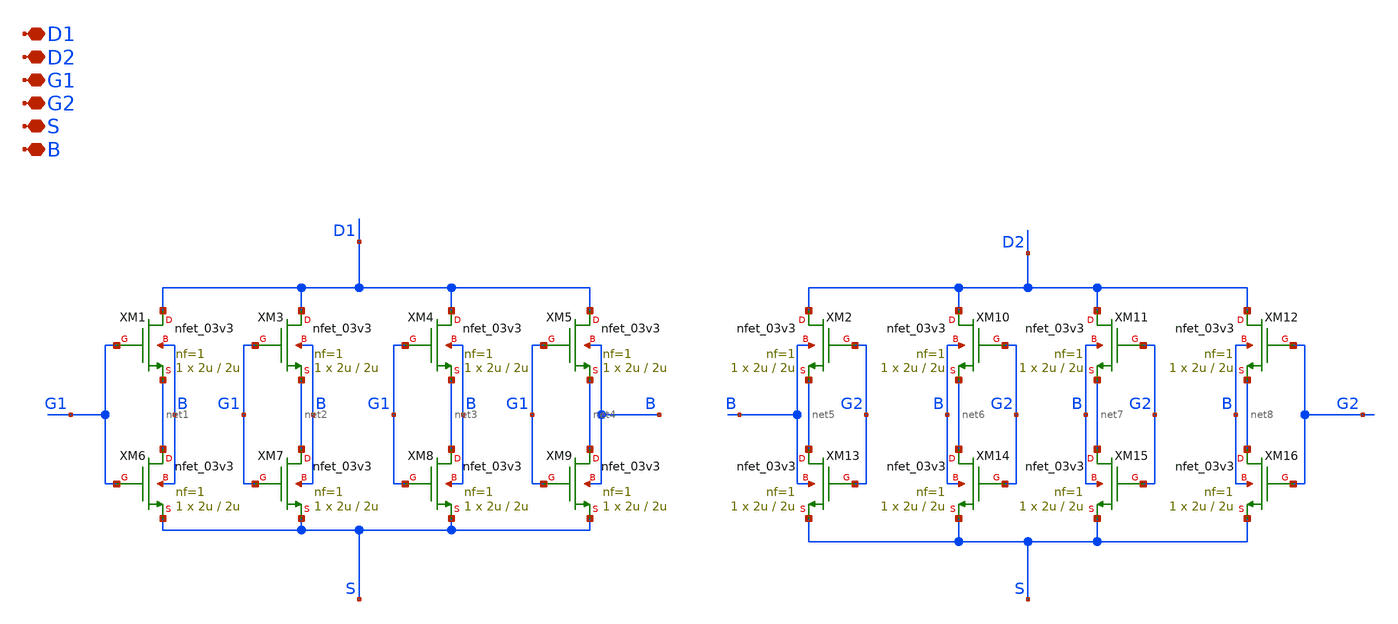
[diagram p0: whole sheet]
** sch_path: TIA/PseudoResistor/DiffN_nfets.sch
**.subckt DiffN_nfets D1 D2 G1 G2 S B
*.iopin D1
*.iopin D2
*.iopin G1
*.iopin G2
*.iopin S
*.iopin B
XM1 D1 G1 net1 B nfet_03v3 L=2u W=2u nf=1 ad='int((nf+1)/2) * W/nf * 0.18u' as='int((nf+2)/2) * W/nf * 0.18u'
+ pd='2*int((nf+1)/2) * (W/nf + 0.18u)' ps='2*int((nf+2)/2) * (W/nf + 0.18u)' nrd='0.18u / W' nrs='0.18u / W'
+ sa=0 sb=0 sd=0 m=1
XM2 D2 G2 net5 B nfet_03v3 L=2u W=2u nf=1 ad='int((nf+1)/2) * W/nf * 0.18u' as='int((nf+2)/2) * W/nf * 0.18u'
+ pd='2*int((nf+1)/2) * (W/nf + 0.18u)' ps='2*int((nf+2)/2) * (W/nf + 0.18u)' nrd='0.18u / W' nrs='0.18u / W'
+ sa=0 sb=0 sd=0 m=1
XM3 D1 G1 net2 B nfet_03v3 L=2u W=2u nf=1 ad='int((nf+1)/2) * W/nf * 0.18u' as='int((nf+2)/2) * W/nf * 0.18u'
+ pd='2*int((nf+1)/2) * (W/nf + 0.18u)' ps='2*int((nf+2)/2) * (W/nf + 0.18u)' nrd='0.18u / W' nrs='0.18u / W'
+ sa=0 sb=0 sd=0 m=1
XM4 D1 G1 net3 B nfet_03v3 L=2u W=2u nf=1 ad='int((nf+1)/2) * W/nf * 0.18u' as='int((nf+2)/2) * W/nf * 0.18u'
+ pd='2*int((nf+1)/2) * (W/nf + 0.18u)' ps='2*int((nf+2)/2) * (W/nf + 0.18u)' nrd='0.18u / W' nrs='0.18u / W'
+ sa=0 sb=0 sd=0 m=1
XM5 D1 G1 net4 B nfet_03v3 L=2u W=2u nf=1 ad='int((nf+1)/2) * W/nf * 0.18u' as='int((nf+2)/2) * W/nf * 0.18u'
+ pd='2*int((nf+1)/2) * (W/nf + 0.18u)' ps='2*int((nf+2)/2) * (W/nf + 0.18u)' nrd='0.18u / W' nrs='0.18u / W'
+ sa=0 sb=0 sd=0 m=1
XM6 net1 G1 S B nfet_03v3 L=2u W=2u nf=1 ad='int((nf+1)/2) * W/nf * 0.18u' as='int((nf+2)/2) * W/nf * 0.18u'
+ pd='2*int((nf+1)/2) * (W/nf + 0.18u)' ps='2*int((nf+2)/2) * (W/nf + 0.18u)' nrd='0.18u / W' nrs='0.18u / W'
+ sa=0 sb=0 sd=0 m=1
XM7 net2 G1 S B nfet_03v3 L=2u W=2u nf=1 ad='int((nf+1)/2) * W/nf * 0.18u' as='int((nf+2)/2) * W/nf * 0.18u'
+ pd='2*int((nf+1)/2) * (W/nf + 0.18u)' ps='2*int((nf+2)/2) * (W/nf + 0.18u)' nrd='0.18u / W' nrs='0.18u / W'
+ sa=0 sb=0 sd=0 m=1
XM8 net3 G1 S B nfet_03v3 L=2u W=2u nf=1 ad='int((nf+1)/2) * W/nf * 0.18u' as='int((nf+2)/2) * W/nf * 0.18u'
+ pd='2*int((nf+1)/2) * (W/nf + 0.18u)' ps='2*int((nf+2)/2) * (W/nf + 0.18u)' nrd='0.18u / W' nrs='0.18u / W'
+ sa=0 sb=0 sd=0 m=1
XM9 net4 G1 S B nfet_03v3 L=2u W=2u nf=1 ad='int((nf+1)/2) * W/nf * 0.18u' as='int((nf+2)/2) * W/nf * 0.18u'
+ pd='2*int((nf+1)/2) * (W/nf + 0.18u)' ps='2*int((nf+2)/2) * (W/nf + 0.18u)' nrd='0.18u / W' nrs='0.18u / W'
+ sa=0 sb=0 sd=0 m=1
XM10 D2 G2 net6 B nfet_03v3 L=2u W=2u nf=1 ad='int((nf+1)/2) * W/nf * 0.18u' as='int((nf+2)/2) * W/nf * 0.18u'
+ pd='2*int((nf+1)/2) * (W/nf + 0.18u)' ps='2*int((nf+2)/2) * (W/nf + 0.18u)' nrd='0.18u / W' nrs='0.18u / W'
+ sa=0 sb=0 sd=0 m=1
XM11 D2 G2 net7 B nfet_03v3 L=2u W=2u nf=1 ad='int((nf+1)/2) * W/nf * 0.18u' as='int((nf+2)/2) * W/nf * 0.18u'
+ pd='2*int((nf+1)/2) * (W/nf + 0.18u)' ps='2*int((nf+2)/2) * (W/nf + 0.18u)' nrd='0.18u / W' nrs='0.18u / W'
+ sa=0 sb=0 sd=0 m=1
XM12 D2 G2 net8 B nfet_03v3 L=2u W=2u nf=1 ad='int((nf+1)/2) * W/nf * 0.18u' as='int((nf+2)/2) * W/nf * 0.18u'
+ pd='2*int((nf+1)/2) * (W/nf + 0.18u)' ps='2*int((nf+2)/2) * (W/nf + 0.18u)' nrd='0.18u / W' nrs='0.18u / W'
+ sa=0 sb=0 sd=0 m=1
XM13 net5 G2 S B nfet_03v3 L=2u W=2u nf=1 ad='int((nf+1)/2) * W/nf * 0.18u' as='int((nf+2)/2) * W/nf * 0.18u'
+ pd='2*int((nf+1)/2) * (W/nf + 0.18u)' ps='2*int((nf+2)/2) * (W/nf + 0.18u)' nrd='0.18u / W' nrs='0.18u / W'
+ sa=0 sb=0 sd=0 m=1
XM14 net6 G2 S B nfet_03v3 L=2u W=2u nf=1 ad='int((nf+1)/2) * W/nf * 0.18u' as='int((nf+2)/2) * W/nf * 0.18u'
+ pd='2*int((nf+1)/2) * (W/nf + 0.18u)' ps='2*int((nf+2)/2) * (W/nf + 0.18u)' nrd='0.18u / W' nrs='0.18u / W'
+ sa=0 sb=0 sd=0 m=1
XM15 net7 G2 S B nfet_03v3 L=2u W=2u nf=1 ad='int((nf+1)/2) * W/nf * 0.18u' as='int((nf+2)/2) * W/nf * 0.18u'
+ pd='2*int((nf+1)/2) * (W/nf + 0.18u)' ps='2*int((nf+2)/2) * (W/nf + 0.18u)' nrd='0.18u / W' nrs='0.18u / W'
+ sa=0 sb=0 sd=0 m=1
XM16 net8 G2 S B nfet_03v3 L=2u W=2u nf=1 ad='int((nf+1)/2) * W/nf * 0.18u' as='int((nf+2)/2) * W/nf * 0.18u'
+ pd='2*int((nf+1)/2) * (W/nf + 0.18u)' ps='2*int((nf+2)/2) * (W/nf + 0.18u)' nrd='0.18u / W' nrs='0.18u / W'
+ sa=0 sb=0 sd=0 m=1
**.ends
.end
